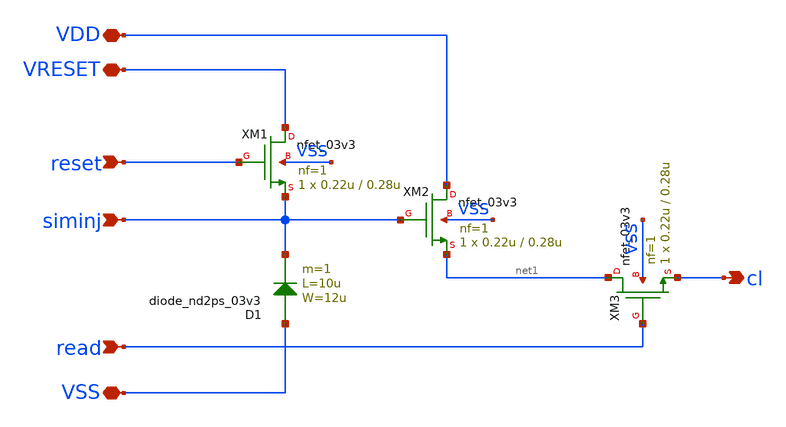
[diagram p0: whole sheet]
** sch_path: xschem/ip_pixel_nw2ps.sch
**.subckt ip_pixel_nw2ps VDD VSS siminj reset read VRESET cl
*.iopin VDD
*.iopin VSS
*.ipin siminj
*.ipin reset
*.ipin read
*.iopin VRESET
*.opin cl
XM1 VRESET reset siminj VSS nfet_03v3 L=0.28u W=0.22u nf=1 ad='int((nf+1)/2) * W/nf * 0.18u' as='int((nf+2)/2) * W/nf * 0.18u'
+ pd='2*int((nf+1)/2) * (W/nf + 0.18u)' ps='2*int((nf+2)/2) * (W/nf + 0.18u)' nrd='0.18u / W' nrs='0.18u / W'
+ sa=0 sb=0 sd=0 m=1
XM2 VDD siminj net1 VSS nfet_03v3 L=0.28u W=0.22u nf=1 ad='int((nf+1)/2) * W/nf * 0.18u' as='int((nf+2)/2) * W/nf * 0.18u'
+ pd='2*int((nf+1)/2) * (W/nf + 0.18u)' ps='2*int((nf+2)/2) * (W/nf + 0.18u)' nrd='0.18u / W' nrs='0.18u / W'
+ sa=0 sb=0 sd=0 m=1
XM3 net1 read cl VSS nfet_03v3 L=0.28u W=0.22u nf=1 ad='int((nf+1)/2) * W/nf * 0.18u' as='int((nf+2)/2) * W/nf * 0.18u'
+ pd='2*int((nf+1)/2) * (W/nf + 0.18u)' ps='2*int((nf+2)/2) * (W/nf + 0.18u)' nrd='0.18u / W' nrs='0.18u / W'
+ sa=0 sb=0 sd=0 m=1
D1 VSS siminj diode_nd2ps_03v3 w=12u l=10u area='12u * 10u ' pj='2*12u + 2*10u ' m=1
**.ends
.end
